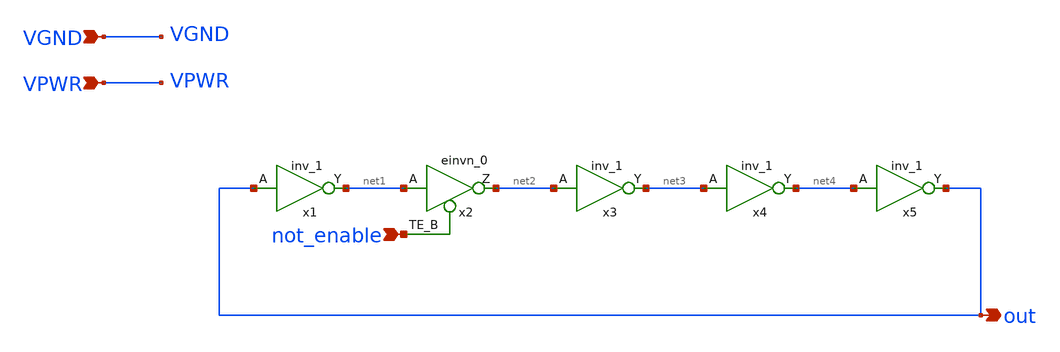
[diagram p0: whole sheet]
** sch_path: xschem/ring_osc.sch
**.subckt ring_osc not_enable VGND VPWR out
*.ipin not_enable
*.ipin VGND
*.ipin VPWR
*.opin out
x1 out VGND VGND VPWR VPWR net1 sky130_fd_sc_hd__inv_1
x2 net1 not_enable VGND VGND VPWR VPWR net2 sky130_fd_sc_hd__einvn_0
x3 net2 VGND VGND VPWR VPWR net3 sky130_fd_sc_hd__inv_1
x4 net3 VGND VGND VPWR VPWR net4 sky130_fd_sc_hd__inv_1
x5 net4 VGND VGND VPWR VPWR out sky130_fd_sc_hd__inv_1
**** begin user architecture code

** opencircuitdesign pdks install
.lib $::SKYWATER_MODELS/sky130.lib.spice tt
.include $::SKYWATER_STDCELLS/sky130_fd_sc_hd.spice





* .options filetype=ascii
Vgnd VGND 0 0
Vpwr VPWR 0 1.8
Venb not_enable 0 0
.control

tran 0.1p 2n uic
write ring_osc.raw
.endc
.end


**** end user architecture code
**.ends
.end
